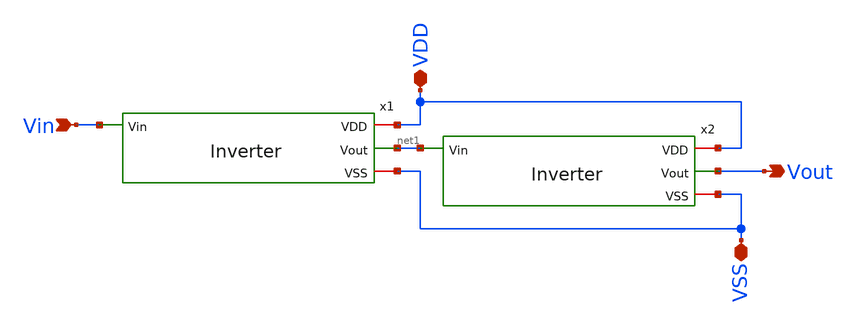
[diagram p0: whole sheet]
** sch_path: xschem/Buffer.sch
**.subckt Buffer VDD VSS Vin Vout
*.iopin VDD
*.iopin VSS
*.ipin Vin
*.opin Vout
x1 VDD Vin net1 VSS Inverter
x2 VDD net1 Vout VSS Inverter
**.ends

* expanding   symbol:  Inverter.sym # of pins=4
** sym_path: xschem/Inverter.sym
** sch_path: xschem/Inverter.sch
.subckt Inverter VDD Vin Vout VSS
*.ipin Vin
*.iopin VDD
*.iopin VSS
*.opin Vout
XM1 Vout Vin VSS VSS sky130_fd_pr__nfet_g5v0d10v5 L=0.5 W=0.75 nf=1 ad='int((nf+1)/2) * W/nf * 0.29'
+ as='int((nf+2)/2) * W/nf * 0.29' pd='2*int((nf+1)/2) * (W/nf + 0.29)' ps='2*int((nf+2)/2) * (W/nf + 0.29)'
+ nrd='0.29 / W' nrs='0.29 / W' sa=0 sb=0 sd=0 mult=1 m=1
XM2 Vout Vin VDD VDD sky130_fd_pr__pfet_g5v0d10v5 L=0.5 W=1.5 nf=1 ad='int((nf+1)/2) * W/nf * 0.29' as='int((nf+2)/2) * W/nf * 0.29'
+ pd='2*int((nf+1)/2) * (W/nf + 0.29)' ps='2*int((nf+2)/2) * (W/nf + 0.29)' nrd='0.29 / W' nrs='0.29 / W'
+ sa=0 sb=0 sd=0 mult=1 m=1
.ends

.end
